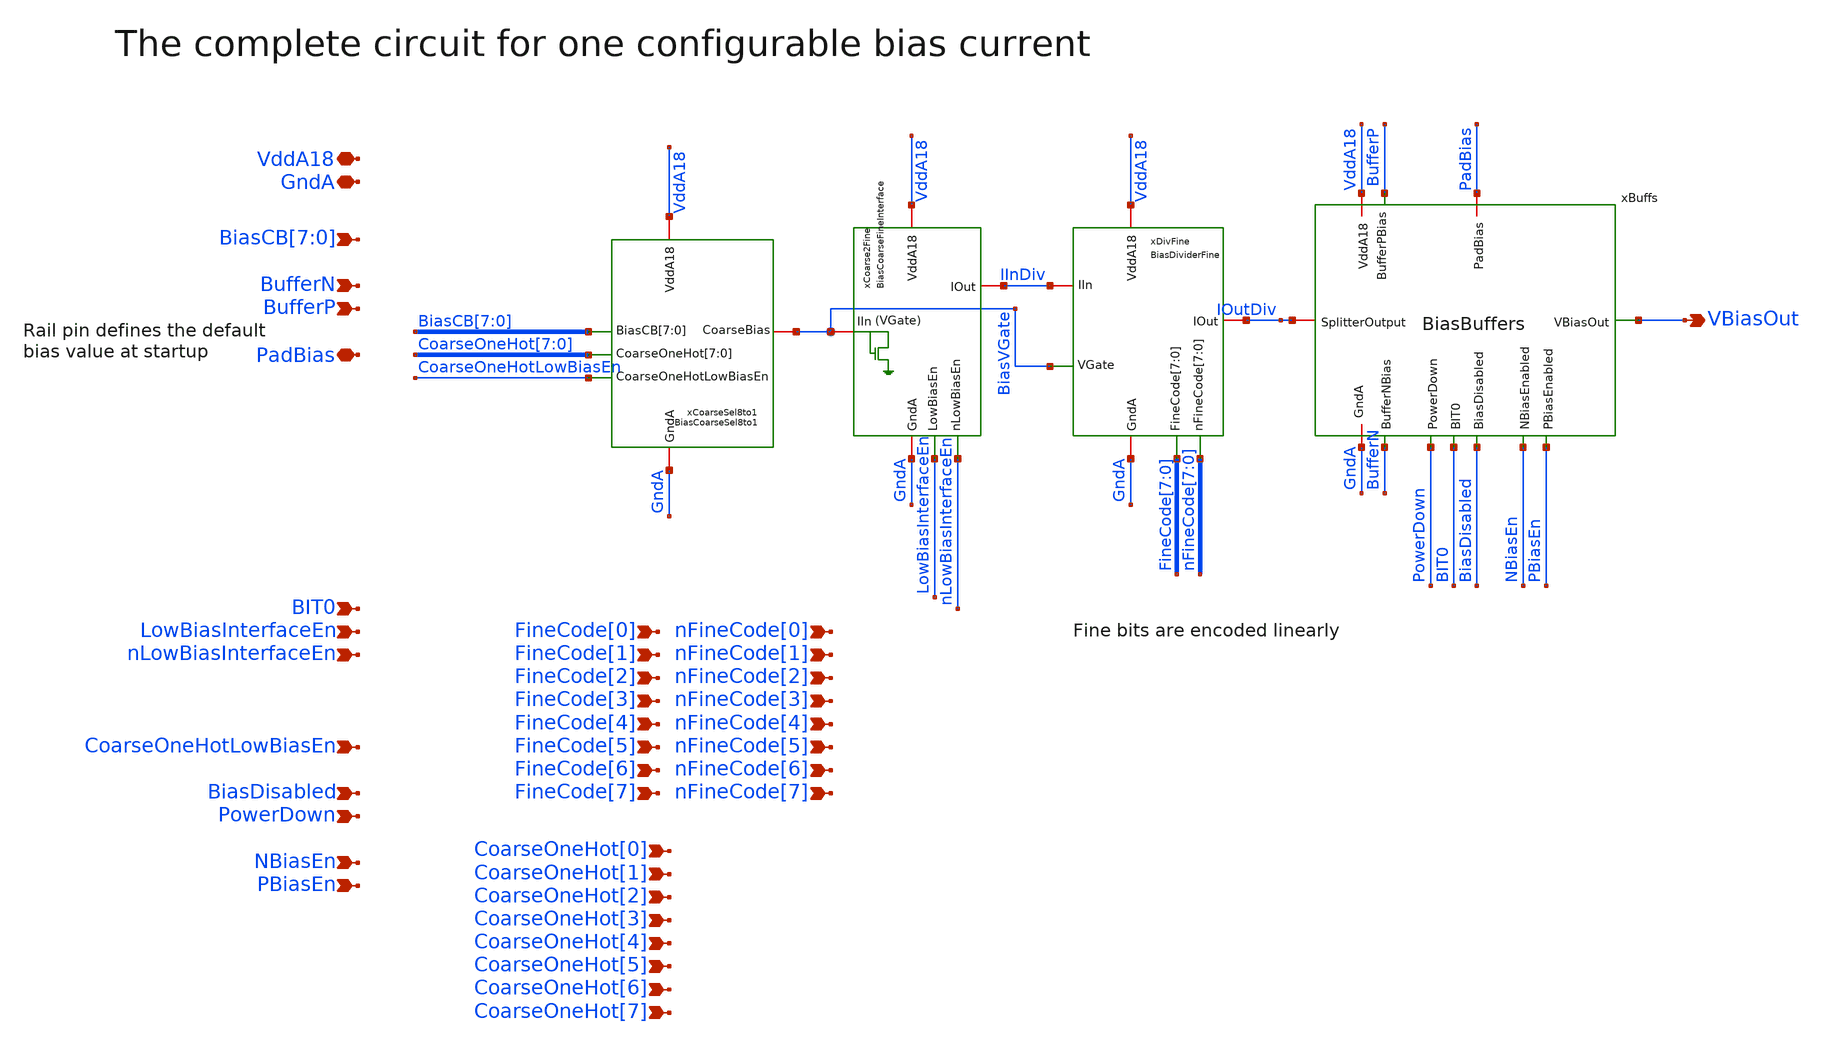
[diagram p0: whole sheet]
** sch_path: analog/klayout/production/final_merge_20260923/testbenches/cace/analog/xschem/BiasBranch.sch
**.subckt BiasBranch VddA18 GndA VBiasOut
*+ BiasCB[7],BiasCB[6],BiasCB[5],BiasCB[4],BiasCB[3],BiasCB[2],BiasCB[1],BiasCB[0] BufferN BufferP LowBiasInterfaceEn nLowBiasInterfaceEn CoarseOneHotLowBiasEn BIT0 BiasDisabled
*+ NBiasEn PBiasEn FineCode[0] FineCode[1] FineCode[2] FineCode[3] FineCode[4] FineCode[5] FineCode[6]
*+ FineCode[7] nFineCode[0] nFineCode[1] nFineCode[2] nFineCode[3] nFineCode[4] nFineCode[5] nFineCode[6]
*+ nFineCode[7] CoarseOneHot[0] CoarseOneHot[1] CoarseOneHot[2] CoarseOneHot[3] CoarseOneHot[4] CoarseOneHot[5]
*+ CoarseOneHot[6] CoarseOneHot[7] PadBias PowerDown
*.iopin VddA18
*.iopin GndA
*.opin VBiasOut
*.ipin BiasCB[7],BiasCB[6],BiasCB[5],BiasCB[4],BiasCB[3],BiasCB[2],BiasCB[1],BiasCB[0]
*.ipin BufferN
*.ipin BufferP
*.ipin LowBiasInterfaceEn
*.ipin nLowBiasInterfaceEn
*.ipin CoarseOneHotLowBiasEn
*.ipin BIT0
*.ipin BiasDisabled
*.ipin NBiasEn
*.ipin PBiasEn
*.ipin FineCode[0]
*.ipin FineCode[1]
*.ipin FineCode[2]
*.ipin FineCode[3]
*.ipin FineCode[4]
*.ipin FineCode[5]
*.ipin FineCode[6]
*.ipin FineCode[7]
*.ipin nFineCode[0]
*.ipin nFineCode[1]
*.ipin nFineCode[2]
*.ipin nFineCode[3]
*.ipin nFineCode[4]
*.ipin nFineCode[5]
*.ipin nFineCode[6]
*.ipin nFineCode[7]
*.ipin CoarseOneHot[0]
*.ipin CoarseOneHot[1]
*.ipin CoarseOneHot[2]
*.ipin CoarseOneHot[3]
*.ipin CoarseOneHot[4]
*.ipin CoarseOneHot[5]
*.ipin CoarseOneHot[6]
*.ipin CoarseOneHot[7]
*.iopin PadBias
*.ipin PowerDown
xCoarse2Fine VddA18 GndA LowBiasInterfaceEn nLowBiasInterfaceEn BiasVGate IInDiv
+ BiasCoarseFineInterface
xDivFine VddA18 GndA FineCode[7] FineCode[6] FineCode[5] FineCode[4] FineCode[3] FineCode[2]
+ FineCode[1] FineCode[0] nFineCode[7] nFineCode[6] nFineCode[5] nFineCode[4] nFineCode[3] nFineCode[2]
+ nFineCode[1] nFineCode[0] IInDiv IOutDiv BiasVGate BiasDividerFine
xBuffs VddA18 GndA NBiasEn PBiasEn BiasDisabled BIT0 BufferN BufferP IOutDiv VBiasOut PadBias
+ PowerDown BiasBuffers
xCoarseSel8to1 VddA18 GndA CoarseOneHot[7] CoarseOneHot[6] CoarseOneHot[5] CoarseOneHot[4]
+ CoarseOneHot[3] CoarseOneHot[2] CoarseOneHot[1] CoarseOneHot[0] CoarseOneHotLowBiasEn BiasCB[7] BiasCB[6] BiasCB[5]
+ BiasCB[4] BiasCB[3] BiasCB[2] BiasCB[1] BiasCB[0] BiasVGate BiasCoarseSel8to1
**.ends
.end
